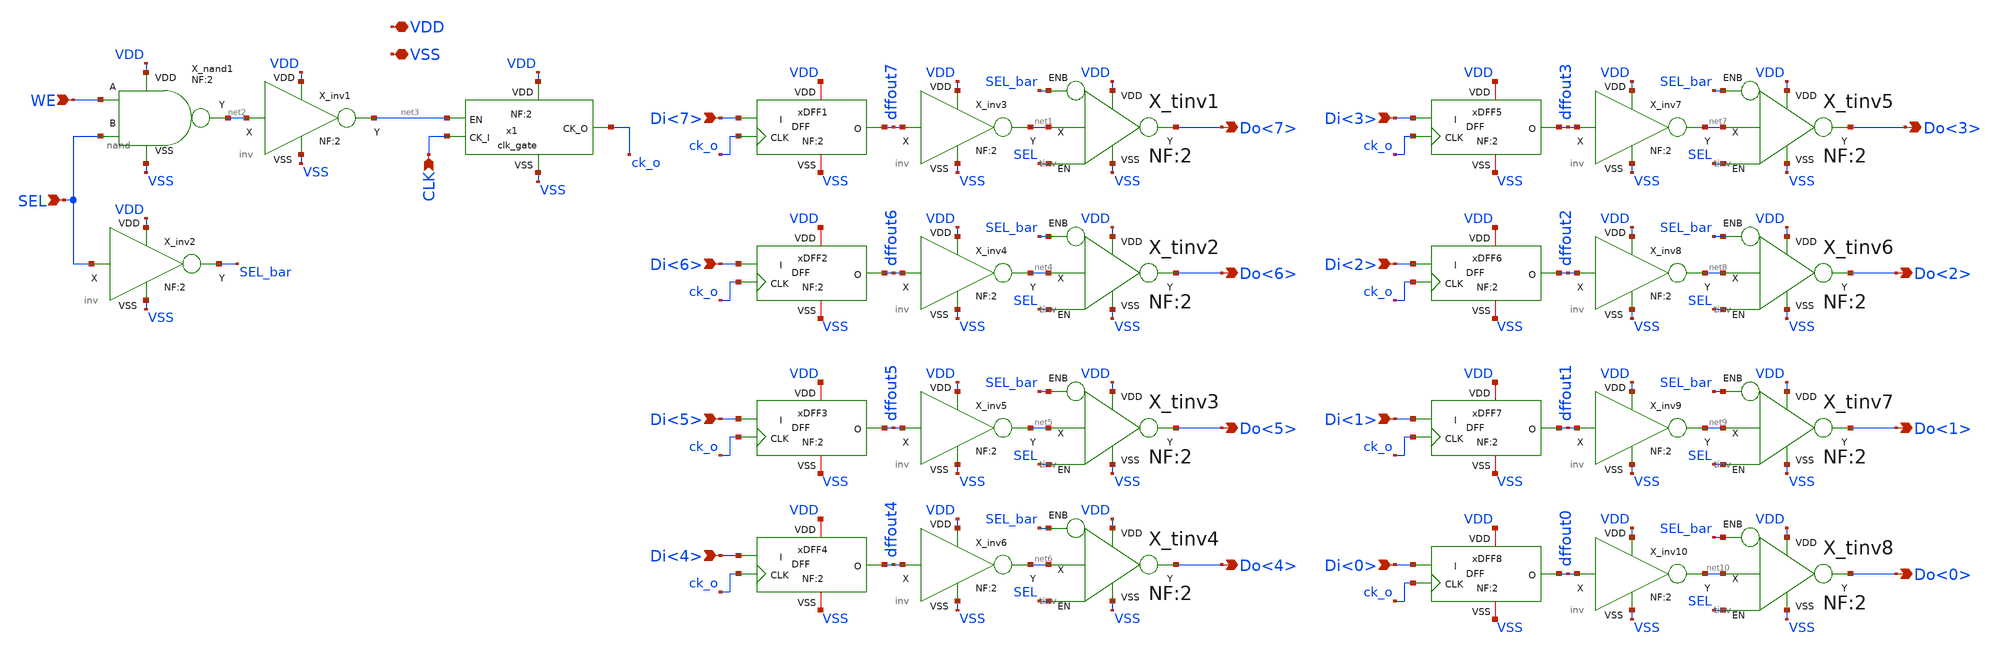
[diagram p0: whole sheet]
** sch_path: xschem_lib/DFFRAM_full_custom/byte_dff.sch
**.subckt byte_dff Do<7> Di<7> Do<6> Di<6> Do<5> Di<5> Do<4> Di<4> Do<3> Di<3> Do<2> Di<2> Do<1>
*+ Di<1> Do<0> Di<0> WE SEL CLK VDD VSS
*.opin Do<7>
*.ipin Di<7>
*.opin Do<6>
*.ipin Di<6>
*.opin Do<5>
*.ipin Di<5>
*.opin Do<4>
*.ipin Di<4>
*.opin Do<3>
*.ipin Di<3>
*.opin Do<2>
*.ipin Di<2>
*.opin Do<1>
*.ipin Di<1>
*.opin Do<0>
*.ipin Di<0>
*.ipin WE
*.ipin SEL
*.ipin CLK
*.iopin VDD
*.iopin VSS
X_nand1 SEL WE net2 VDD VSS nand NF=2
X_inv1 net2 VDD VSS net3 inv NF=2
X_inv2 SEL VDD VSS SEL_bar inv NF=2
x1 VDD net3 ck_o CLK VSS clk_gate NF=2
xDFF1 VDD VSS Di<7> dffout7 ck_o DFF NF=2
X_tinv1 net1 SEL SEL_bar VDD VSS Do<7> tinv NF=2
X_inv3 dffout7 VDD VSS net1 inv NF=2
xDFF2 VDD VSS Di<6> dffout6 ck_o DFF NF=2
xDFF3 VDD VSS Di<5> dffout5 ck_o DFF NF=2
xDFF4 VDD VSS Di<4> dffout4 ck_o DFF NF=2
xDFF5 VDD VSS Di<3> dffout3 ck_o DFF NF=2
xDFF6 VDD VSS Di<2> dffout2 ck_o DFF NF=2
xDFF7 VDD VSS Di<1> dffout1 ck_o DFF NF=2
xDFF8 VDD VSS Di<0> dffout0 ck_o DFF NF=2
X_tinv2 net4 SEL SEL_bar VDD VSS Do<6> tinv NF=2
X_inv4 dffout6 VDD VSS net4 inv NF=2
X_tinv3 net5 SEL SEL_bar VDD VSS Do<5> tinv NF=2
X_inv5 dffout5 VDD VSS net5 inv NF=2
X_tinv4 net6 SEL SEL_bar VDD VSS Do<4> tinv NF=2
X_inv6 dffout4 VDD VSS net6 inv NF=2
X_tinv5 net7 SEL SEL_bar VDD VSS Do<3> tinv NF=2
X_inv7 dffout3 VDD VSS net7 inv NF=2
X_tinv6 net8 SEL SEL_bar VDD VSS Do<2> tinv NF=2
X_inv8 dffout2 VDD VSS net8 inv NF=2
X_tinv7 net9 SEL SEL_bar VDD VSS Do<1> tinv NF=2
X_inv9 dffout1 VDD VSS net9 inv NF=2
X_tinv8 net10 SEL SEL_bar VDD VSS Do<0> tinv NF=2
X_inv10 dffout0 VDD VSS net10 inv NF=2
**.ends
.end
